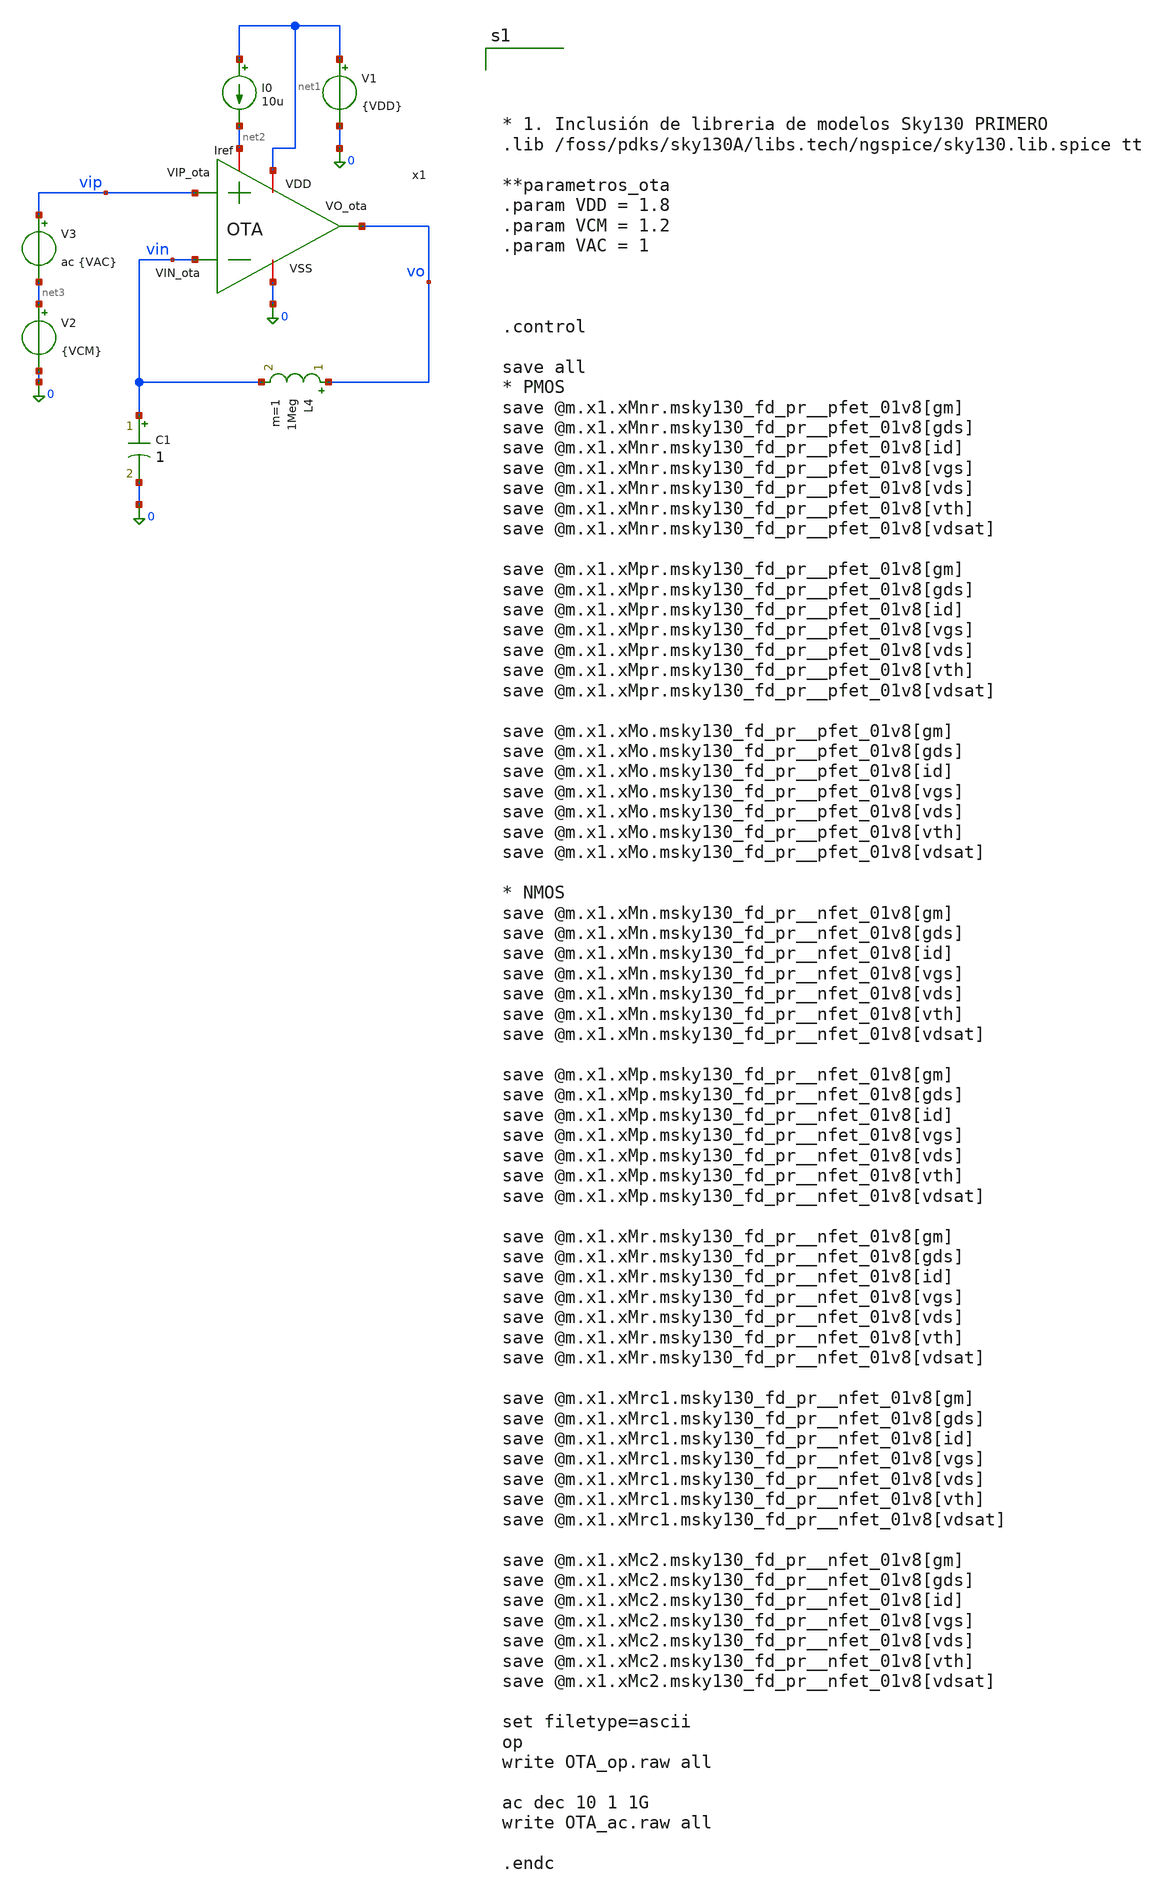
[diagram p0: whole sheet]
** sch_path: xschem/OTA_tbtran.sch
**.subckt OTA_tbtran
x1 net1 vo vin vip net2 0 OTA
V1 net1 0 {VDD}
I0 net1 net2 10u
V2 net3 0 {VCM}
V3 vip net3 ac {VAC}
L4 vo vin 1Meg m=1
C1 vin 0 1 m=1
**** begin user architecture code




* 1. Inclusión de libreria de modelos Sky130 PRIMERO
.lib /foss/pdks/sky130A/libs.tech/ngspice/sky130.lib.spice tt

**parametros_ota
.param VDD = 1.8
.param VCM = 1.2
.param VAC = 1



.control

save all
* PMOS
save @m.x1.xMnr.msky130_fd_pr__pfet_01v8[gm]
save @m.x1.xMnr.msky130_fd_pr__pfet_01v8[gds]
save @m.x1.xMnr.msky130_fd_pr__pfet_01v8[id]
save @m.x1.xMnr.msky130_fd_pr__pfet_01v8[vgs]
save @m.x1.xMnr.msky130_fd_pr__pfet_01v8[vds]
save @m.x1.xMnr.msky130_fd_pr__pfet_01v8[vth]
save @m.x1.xMnr.msky130_fd_pr__pfet_01v8[vdsat]

save @m.x1.xMpr.msky130_fd_pr__pfet_01v8[gm]
save @m.x1.xMpr.msky130_fd_pr__pfet_01v8[gds]
save @m.x1.xMpr.msky130_fd_pr__pfet_01v8[id]
save @m.x1.xMpr.msky130_fd_pr__pfet_01v8[vgs]
save @m.x1.xMpr.msky130_fd_pr__pfet_01v8[vds]
save @m.x1.xMpr.msky130_fd_pr__pfet_01v8[vth]
save @m.x1.xMpr.msky130_fd_pr__pfet_01v8[vdsat]

save @m.x1.xMo.msky130_fd_pr__pfet_01v8[gm]
save @m.x1.xMo.msky130_fd_pr__pfet_01v8[gds]
save @m.x1.xMo.msky130_fd_pr__pfet_01v8[id]
save @m.x1.xMo.msky130_fd_pr__pfet_01v8[vgs]
save @m.x1.xMo.msky130_fd_pr__pfet_01v8[vds]
save @m.x1.xMo.msky130_fd_pr__pfet_01v8[vth]
save @m.x1.xMo.msky130_fd_pr__pfet_01v8[vdsat]

* NMOS
save @m.x1.xMn.msky130_fd_pr__nfet_01v8[gm]
save @m.x1.xMn.msky130_fd_pr__nfet_01v8[gds]
save @m.x1.xMn.msky130_fd_pr__nfet_01v8[id]
save @m.x1.xMn.msky130_fd_pr__nfet_01v8[vgs]
save @m.x1.xMn.msky130_fd_pr__nfet_01v8[vds]
save @m.x1.xMn.msky130_fd_pr__nfet_01v8[vth]
save @m.x1.xMn.msky130_fd_pr__nfet_01v8[vdsat]

save @m.x1.xMp.msky130_fd_pr__nfet_01v8[gm]
save @m.x1.xMp.msky130_fd_pr__nfet_01v8[gds]
save @m.x1.xMp.msky130_fd_pr__nfet_01v8[id]
save @m.x1.xMp.msky130_fd_pr__nfet_01v8[vgs]
save @m.x1.xMp.msky130_fd_pr__nfet_01v8[vds]
save @m.x1.xMp.msky130_fd_pr__nfet_01v8[vth]
save @m.x1.xMp.msky130_fd_pr__nfet_01v8[vdsat]

save @m.x1.xMr.msky130_fd_pr__nfet_01v8[gm]
save @m.x1.xMr.msky130_fd_pr__nfet_01v8[gds]
save @m.x1.xMr.msky130_fd_pr__nfet_01v8[id]
save @m.x1.xMr.msky130_fd_pr__nfet_01v8[vgs]
save @m.x1.xMr.msky130_fd_pr__nfet_01v8[vds]
save @m.x1.xMr.msky130_fd_pr__nfet_01v8[vth]
save @m.x1.xMr.msky130_fd_pr__nfet_01v8[vdsat]

save @m.x1.xMrc1.msky130_fd_pr__nfet_01v8[gm]
save @m.x1.xMrc1.msky130_fd_pr__nfet_01v8[gds]
save @m.x1.xMrc1.msky130_fd_pr__nfet_01v8[id]
save @m.x1.xMrc1.msky130_fd_pr__nfet_01v8[vgs]
save @m.x1.xMrc1.msky130_fd_pr__nfet_01v8[vds]
save @m.x1.xMrc1.msky130_fd_pr__nfet_01v8[vth]
save @m.x1.xMrc1.msky130_fd_pr__nfet_01v8[vdsat]

save @m.x1.xMc2.msky130_fd_pr__nfet_01v8[gm]
save @m.x1.xMc2.msky130_fd_pr__nfet_01v8[gds]
save @m.x1.xMc2.msky130_fd_pr__nfet_01v8[id]
save @m.x1.xMc2.msky130_fd_pr__nfet_01v8[vgs]
save @m.x1.xMc2.msky130_fd_pr__nfet_01v8[vds]
save @m.x1.xMc2.msky130_fd_pr__nfet_01v8[vth]
save @m.x1.xMc2.msky130_fd_pr__nfet_01v8[vdsat]

set filetype=ascii
op
write OTA_op.raw all

ac dec 10 1 1G
write OTA_ac.raw all

.endc


**** end user architecture code
**.ends

* expanding   symbol:  /foss/designs/LDO-sky130/xschem/OTA.sym # of pins=6
** sym_path: xschem/OTA.sym
** sch_path: xschem/OTA.sch
.subckt OTA VDD VO_ota VIN_ota VIP_ota Iref VSS
*.ipin VIN_ota
*.opin VO_ota
*.iopin Iref
*.iopin VSS
*.iopin VDD
*.ipin VIP_ota
XMr Iref Iref VSS VSS sky130_fd_pr__nfet_01v8 L=0.15 W=1 nf=1 ad='int((1 + 1)/2) * 1 / 1 * 0.29' as='int((1 + 2)/2) * 1 / 1 * 0.29'
+ pd='2*int((1 + 1)/2) * (1 / 1 + 0.29)' ps='2*int((1 + 2)/2) * (1 / 1 + 0.29)' nrd='0.29 / 1 ' nrs='0.29 / 1 '
+ sa=0 sb=0 sd=0 mult=1 m=1
XMo VO_ota VO_ota VDD VDD sky130_fd_pr__pfet_01v8 L=0.15 W=1 nf=1 ad='int((1 + 1)/2) * 1 / 1 * 0.29'
+ as='int((1 + 2)/2) * 1 / 1 * 0.29' pd='2*int((1 + 1)/2) * (1 / 1 + 0.29)' ps='2*int((1 + 2)/2) * (1 / 1 + 0.29)'
+ nrd='0.29 / 1 ' nrs='0.29 / 1 ' sa=0 sb=0 sd=0 mult=1 m=1
XMrc1 Vtail Iref VSS VSS sky130_fd_pr__nfet_01v8 L=0.15 W=1 nf=1 ad='int((1 + 1)/2) * 1 / 1 * 0.29' as='int((1 + 2)/2) * 1 / 1 * 0.29'
+ pd='2*int((1 + 1)/2) * (1 / 1 + 0.29)' ps='2*int((1 + 2)/2) * (1 / 1 + 0.29)' nrd='0.29 / 1 ' nrs='0.29 / 1 '
+ sa=0 sb=0 sd=0 mult=1 m=1
XMc2 VO_ota Iref VSS VSS sky130_fd_pr__nfet_01v8 L=0.15 W=1 nf=1 ad='int((1 + 1)/2) * 1 / 1 * 0.29' as='int((1 + 2)/2) * 1 / 1 * 0.29'
+ pd='2*int((1 + 1)/2) * (1 / 1 + 0.29)' ps='2*int((1 + 2)/2) * (1 / 1 + 0.29)' nrd='0.29 / 1 ' nrs='0.29 / 1 '
+ sa=0 sb=0 sd=0 mult=1 m=1
XMn VGP VIN_ota Vtail VSS sky130_fd_pr__nfet_01v8 L=0.15 W=1 nf=1 ad='int((1 + 1)/2) * 1 / 1 * 0.29'
+ as='int((1 + 2)/2) * 1 / 1 * 0.29' pd='2*int((1 + 1)/2) * (1 / 1 + 0.29)' ps='2*int((1 + 2)/2) * (1 / 1 + 0.29)'
+ nrd='0.29 / 1 ' nrs='0.29 / 1 ' sa=0 sb=0 sd=0 mult=1 m=1
XMp VO_ota VIP_ota Vtail VSS sky130_fd_pr__nfet_01v8 L=0.15 W=1 nf=1 ad='int((1 + 1)/2) * 1 / 1 * 0.29'
+ as='int((1 + 2)/2) * 1 / 1 * 0.29' pd='2*int((1 + 1)/2) * (1 / 1 + 0.29)' ps='2*int((1 + 2)/2) * (1 / 1 + 0.29)'
+ nrd='0.29 / 1 ' nrs='0.29 / 1 ' sa=0 sb=0 sd=0 mult=1 m=1
XMpr VO_ota VGP VDD VDD sky130_fd_pr__pfet_01v8 L=0.15 W=1 nf=1 ad='int((1 + 1)/2) * 1 / 1 * 0.29' as='int((1 + 2)/2) * 1 / 1 * 0.29'
+ pd='2*int((1 + 1)/2) * (1 / 1 + 0.29)' ps='2*int((1 + 2)/2) * (1 / 1 + 0.29)' nrd='0.29 / 1 ' nrs='0.29 / 1 '
+ sa=0 sb=0 sd=0 mult=1 m=1
XMnr VGP VGP VDD VDD sky130_fd_pr__pfet_01v8 L=0.15 W=1 nf=1 ad='int((1 + 1)/2) * 1 / 1 * 0.29' as='int((1 + 2)/2) * 1 / 1 * 0.29'
+ pd='2*int((1 + 1)/2) * (1 / 1 + 0.29)' ps='2*int((1 + 2)/2) * (1 / 1 + 0.29)' nrd='0.29 / 1 ' nrs='0.29 / 1 '
+ sa=0 sb=0 sd=0 mult=1 m=1
.ends

.end
